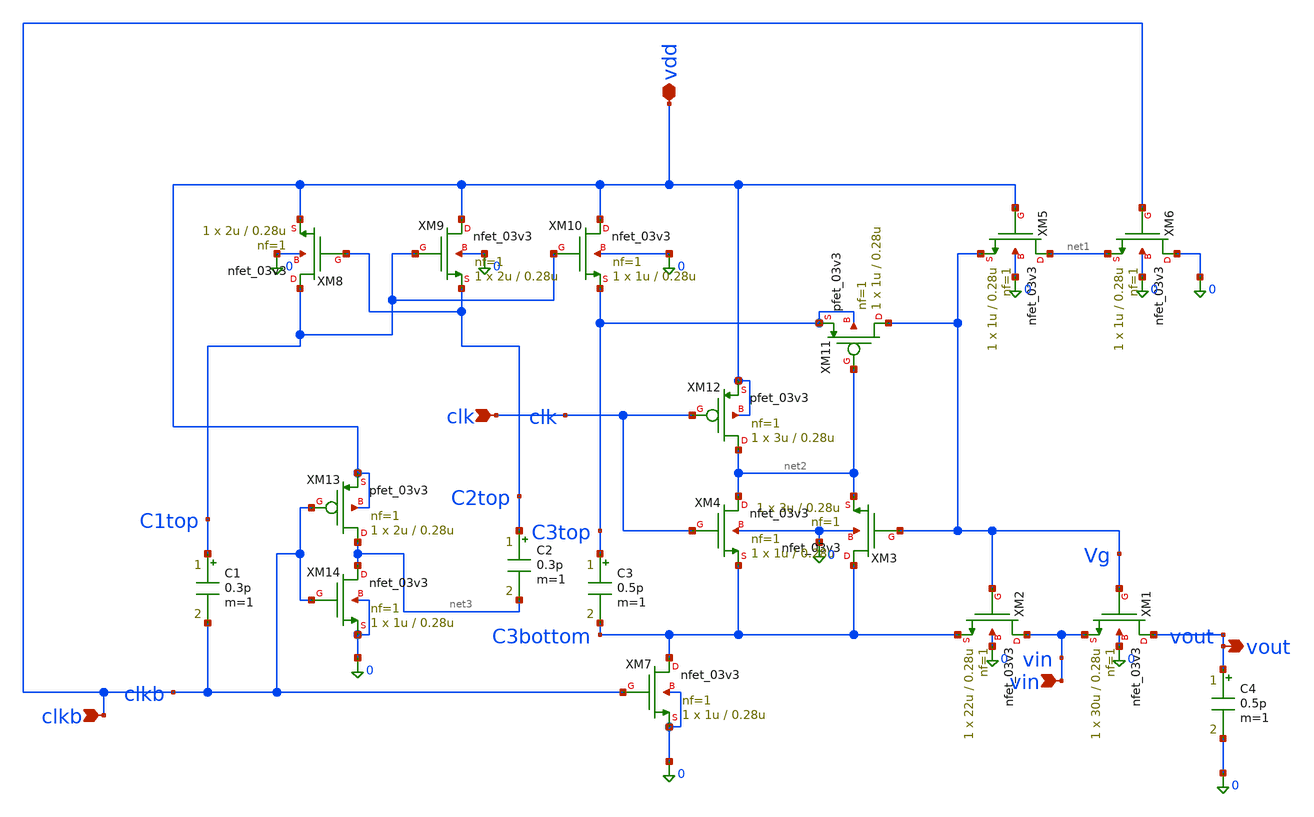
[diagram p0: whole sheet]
** sch_path: analog/blocks/Bootstrapped_Switch/bootstrapped_switch.sch
**.subckt bootstrapped_switch clk clkb vin vdd vout
*.ipin clk
*.ipin clkb
*.ipin vin
*.iopin vdd
*.opin vout
XM1 vout Vg vin 0 nfet_03v3 L=0.28u W=30u nf=1 ad='int((nf+1)/2) * W/nf * 0.18u' as='int((nf+2)/2) * W/nf * 0.18u'
+ pd='2*int((nf+1)/2) * (W/nf + 0.18u)' ps='2*int((nf+2)/2) * (W/nf + 0.18u)' nrd='0.18u / W' nrs='0.18u / W'
+ sa=0 sb=0 sd=0 m=1
XM2 vin Vg C3bottom 0 nfet_03v3 L=0.28u W=22u nf=1 ad='int((nf+1)/2) * W/nf * 0.18u' as='int((nf+2)/2) * W/nf * 0.18u'
+ pd='2*int((nf+1)/2) * (W/nf + 0.18u)' ps='2*int((nf+2)/2) * (W/nf + 0.18u)' nrd='0.18u / W' nrs='0.18u / W'
+ sa=0 sb=0 sd=0 m=1
XM3 C3bottom Vg net2 0 nfet_03v3 L=0.28u W=3u nf=1 ad='int((nf+1)/2) * W/nf * 0.18u' as='int((nf+2)/2) * W/nf * 0.18u'
+ pd='2*int((nf+1)/2) * (W/nf + 0.18u)' ps='2*int((nf+2)/2) * (W/nf + 0.18u)' nrd='0.18u / W' nrs='0.18u / W'
+ sa=0 sb=0 sd=0 m=1
XM4 net2 clk C3bottom 0 nfet_03v3 L=0.28u W=1u nf=1 ad='int((nf+1)/2) * W/nf * 0.18u' as='int((nf+2)/2) * W/nf * 0.18u'
+ pd='2*int((nf+1)/2) * (W/nf + 0.18u)' ps='2*int((nf+2)/2) * (W/nf + 0.18u)' nrd='0.18u / W' nrs='0.18u / W'
+ sa=0 sb=0 sd=0 m=1
XM5 net1 vdd Vg 0 nfet_03v3 L=0.28u W=1u nf=1 ad='int((nf+1)/2) * W/nf * 0.18u' as='int((nf+2)/2) * W/nf * 0.18u'
+ pd='2*int((nf+1)/2) * (W/nf + 0.18u)' ps='2*int((nf+2)/2) * (W/nf + 0.18u)' nrd='0.18u / W' nrs='0.18u / W'
+ sa=0 sb=0 sd=0 m=1
XM6 0 clkb net1 0 nfet_03v3 L=0.28u W=1u nf=1 ad='int((nf+1)/2) * W/nf * 0.18u' as='int((nf+2)/2) * W/nf * 0.18u'
+ pd='2*int((nf+1)/2) * (W/nf + 0.18u)' ps='2*int((nf+2)/2) * (W/nf + 0.18u)' nrd='0.18u / W' nrs='0.18u / W'
+ sa=0 sb=0 sd=0 m=1
XM7 C3bottom clkb 0 0 nfet_03v3 L=0.28u W=1u nf=1 ad='int((nf+1)/2) * W/nf * 0.18u' as='int((nf+2)/2) * W/nf * 0.18u'
+ pd='2*int((nf+1)/2) * (W/nf + 0.18u)' ps='2*int((nf+2)/2) * (W/nf + 0.18u)' nrd='0.18u / W' nrs='0.18u / W'
+ sa=0 sb=0 sd=0 m=1
XM8 C1top C2top vdd 0 nfet_03v3 L=0.28u W=2u nf=1 ad='int((nf+1)/2) * W/nf * 0.18u' as='int((nf+2)/2) * W/nf * 0.18u'
+ pd='2*int((nf+1)/2) * (W/nf + 0.18u)' ps='2*int((nf+2)/2) * (W/nf + 0.18u)' nrd='0.18u / W' nrs='0.18u / W'
+ sa=0 sb=0 sd=0 m=1
XM9 vdd C1top C2top 0 nfet_03v3 L=0.28u W=2u nf=1 ad='int((nf+1)/2) * W/nf * 0.18u' as='int((nf+2)/2) * W/nf * 0.18u'
+ pd='2*int((nf+1)/2) * (W/nf + 0.18u)' ps='2*int((nf+2)/2) * (W/nf + 0.18u)' nrd='0.18u / W' nrs='0.18u / W'
+ sa=0 sb=0 sd=0 m=1
XM10 vdd C1top C3top 0 nfet_03v3 L=0.28u W=1u nf=1 ad='int((nf+1)/2) * W/nf * 0.18u' as='int((nf+2)/2) * W/nf * 0.18u'
+ pd='2*int((nf+1)/2) * (W/nf + 0.18u)' ps='2*int((nf+2)/2) * (W/nf + 0.18u)' nrd='0.18u / W' nrs='0.18u / W'
+ sa=0 sb=0 sd=0 m=1
XM11 Vg net2 C3top C3top pfet_03v3 L=0.28u W=1u nf=1 ad='int((nf+1)/2) * W/nf * 0.18u' as='int((nf+2)/2) * W/nf * 0.18u'
+ pd='2*int((nf+1)/2) * (W/nf + 0.18u)' ps='2*int((nf+2)/2) * (W/nf + 0.18u)' nrd='0.18u / W' nrs='0.18u / W'
+ sa=0 sb=0 sd=0 m=1
XM12 net2 clk vdd vdd pfet_03v3 L=0.28u W=3u nf=1 ad='int((nf+1)/2) * W/nf * 0.18u' as='int((nf+2)/2) * W/nf * 0.18u'
+ pd='2*int((nf+1)/2) * (W/nf + 0.18u)' ps='2*int((nf+2)/2) * (W/nf + 0.18u)' nrd='0.18u / W' nrs='0.18u / W'
+ sa=0 sb=0 sd=0 m=1
C1 C1top clkb 0.3p m=1
C2 C2top net3 0.3p m=1
C3 C3top C3bottom 0.5p m=1
XM13 net3 clkb vdd vdd pfet_03v3 L=0.28u W=2u nf=1 ad='int((nf+1)/2) * W/nf * 0.18u' as='int((nf+2)/2) * W/nf * 0.18u'
+ pd='2*int((nf+1)/2) * (W/nf + 0.18u)' ps='2*int((nf+2)/2) * (W/nf + 0.18u)' nrd='0.18u / W' nrs='0.18u / W'
+ sa=0 sb=0 sd=0 m=1
XM14 net3 clkb 0 0 nfet_03v3 L=0.28u W=1u nf=1 ad='int((nf+1)/2) * W/nf * 0.18u' as='int((nf+2)/2) * W/nf * 0.18u'
+ pd='2*int((nf+1)/2) * (W/nf + 0.18u)' ps='2*int((nf+2)/2) * (W/nf + 0.18u)' nrd='0.18u / W' nrs='0.18u / W'
+ sa=0 sb=0 sd=0 m=1
C4 vout 0 0.5p m=1
**.ends
.end
